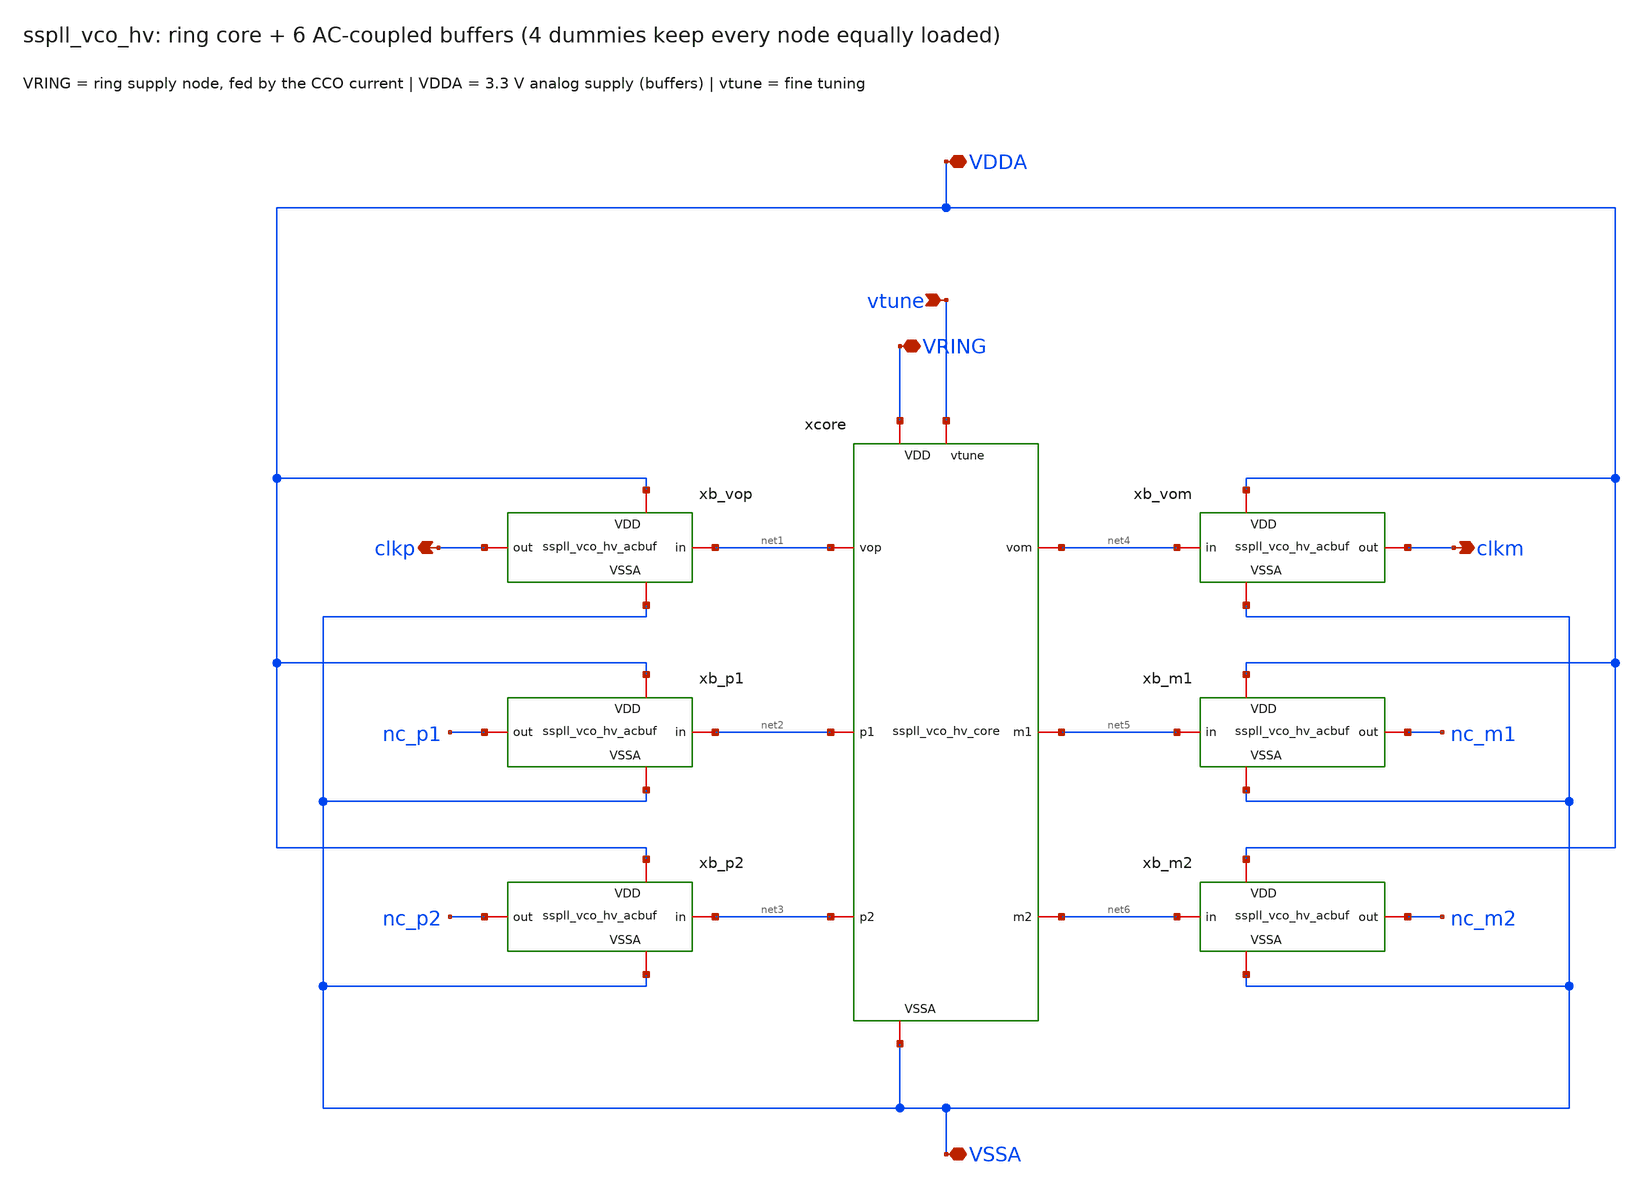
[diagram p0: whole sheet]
** sch_path: xschem/vco_hv/sspll_vco_hv.sch
**.subckt sspll_vco_hv VRING vtune VDDA VSSA clkp clkm
*.iopin VRING
*.ipin vtune
*.iopin VDDA
*.iopin VSSA
*.opin clkp
*.opin clkm
xcore net1 net2 net3 net4 net5 net6 VRING vtune VSSA sspll_vco_hv_core
xb_vop net1 clkp VDDA VSSA sspll_vco_hv_acbuf
xb_p1 net2 nc_p1 VDDA VSSA sspll_vco_hv_acbuf
xb_p2 net3 nc_p2 VDDA VSSA sspll_vco_hv_acbuf
xb_vom net4 clkm VDDA VSSA sspll_vco_hv_acbuf
xb_m1 net5 nc_m1 VDDA VSSA sspll_vco_hv_acbuf
xb_m2 net6 nc_m2 VDDA VSSA sspll_vco_hv_acbuf
**.ends

* expanding   symbol:  sspll_vco_hv_core.sym # of pins=9
** sym_path: xschem/vco_hv/sspll_vco_hv_core.sym
** sch_path: xschem/vco_hv/sspll_vco_hv_core.sch
.subckt sspll_vco_hv_core vop p1 p2 vom m1 m2 VDD vtune VSSA
*.iopin VDD
*.ipin vtune
*.iopin VSSA
*.iopin p1
*.iopin m1
*.iopin p2
*.iopin m2
*.iopin vop
*.iopin vom
x1 vop vom p1 m1 VDD vtune VSSA sspll_vco_hv_dcell
x2 p1 m1 p2 m2 VDD vtune VSSA sspll_vco_hv_dcell
x3 p2 m2 vom vop VDD vtune VSSA sspll_vco_hv_dcell
.ends


* expanding   symbol:  sspll_vco_hv_acbuf.sym # of pins=4
** sym_path: xschem/vco_hv/sspll_vco_hv_acbuf.sym
** sch_path: xschem/vco_hv/sspll_vco_hv_acbuf.sch
.subckt sspll_vco_hv_acbuf in out VDD VSSA
*.iopin VDD
*.iopin VSSA
*.ipin in
*.opin out
XXCC net1 in sky130_fd_pr__cap_mim_m3_1 W=4.2 L=4.2 MF=1 m=1
XXP1 net2 net1 VDD VDD sky130_fd_pr__pfet_g5v0d10v5 L=0.5 W=1.5 nf=1 ad='int((nf+1)/2) * W/nf * 0.29'
+ as='int((nf+2)/2) * W/nf * 0.29' pd='2*int((nf+1)/2) * (W/nf + 0.29)' ps='2*int((nf+2)/2) * (W/nf + 0.29)'
+ nrd='0.29 / W' nrs='0.29 / W' sa=0 sb=0 sd=0 mult=1 m=1
XXN1 net2 net1 VSSA VSSA sky130_fd_pr__nfet_g5v0d10v5 L=0.5 W=0.6 nf=1 ad='int((nf+1)/2) * W/nf * 0.29'
+ as='int((nf+2)/2) * W/nf * 0.29' pd='2*int((nf+1)/2) * (W/nf + 0.29)' ps='2*int((nf+2)/2) * (W/nf + 0.29)'
+ nrd='0.29 / W' nrs='0.29 / W' sa=0 sb=0 sd=0 mult=1 m=1
XXRF net2 net1 VSSA sky130_fd_pr__res_xhigh_po_0p35 L=39.8 mult=1 m=1
XXP2 out net2 VDD VDD sky130_fd_pr__pfet_g5v0d10v5 L=0.5 W=3 nf=1 ad='int((nf+1)/2) * W/nf * 0.29' as='int((nf+2)/2) * W/nf * 0.29'
+ pd='2*int((nf+1)/2) * (W/nf + 0.29)' ps='2*int((nf+2)/2) * (W/nf + 0.29)' nrd='0.29 / W' nrs='0.29 / W'
+ sa=0 sb=0 sd=0 mult=1 m=1
XXN2 out net2 VSSA VSSA sky130_fd_pr__nfet_g5v0d10v5 L=0.5 W=1.2 nf=1 ad='int((nf+1)/2) * W/nf * 0.29'
+ as='int((nf+2)/2) * W/nf * 0.29' pd='2*int((nf+1)/2) * (W/nf + 0.29)' ps='2*int((nf+2)/2) * (W/nf + 0.29)'
+ nrd='0.29 / W' nrs='0.29 / W' sa=0 sb=0 sd=0 mult=1 m=1
.ends


* expanding   symbol:  sspll_vco_hv_dcell.sym # of pins=7
** sym_path: xschem/vco_hv/sspll_vco_hv_dcell.sym
** sch_path: xschem/vco_hv/sspll_vco_hv_dcell.sch
.subckt sspll_vco_hv_dcell inp inm outp outm VDD vtune VSSA
*.iopin VDD
*.iopin VSSA
*.ipin vtune
*.ipin inp
*.ipin inm
*.opin outm
*.opin outp
XXP1 outm inp VDD VDD sky130_fd_pr__pfet_g5v0d10v5 L=0.5 W=25 nf=5 ad='int((nf+1)/2) * W/nf * 0.29' as='int((nf+2)/2) * W/nf * 0.29'
+ pd='2*int((nf+1)/2) * (W/nf + 0.29)' ps='2*int((nf+2)/2) * (W/nf + 0.29)' nrd='0.29 / W' nrs='0.29 / W'
+ sa=0 sb=0 sd=0 mult=1 m=1
XXN1 outm inp VSSA VSSA sky130_fd_pr__nfet_g5v0d10v5 L=0.5 W=7.5 nf=2 ad='int((nf+1)/2) * W/nf * 0.29'
+ as='int((nf+2)/2) * W/nf * 0.29' pd='2*int((nf+1)/2) * (W/nf + 0.29)' ps='2*int((nf+2)/2) * (W/nf + 0.29)'
+ nrd='0.29 / W' nrs='0.29 / W' sa=0 sb=0 sd=0 mult=1 m=1
XXS1 outm vtune net1 VSSA sky130_fd_pr__nfet_g5v0d10v5 L=1.0 W=10 nf=2 ad='int((nf+1)/2) * W/nf * 0.29'
+ as='int((nf+2)/2) * W/nf * 0.29' pd='2*int((nf+1)/2) * (W/nf + 0.29)' ps='2*int((nf+2)/2) * (W/nf + 0.29)'
+ nrd='0.29 / W' nrs='0.29 / W' sa=0 sb=0 sd=0 mult=1 m=1
XXC1 VSSA net1 VSSA VSSA sky130_fd_pr__nfet_g5v0d10v5 L=1.0 W=6.25 nf=1 ad='int((nf+1)/2) * W/nf * 0.29'
+ as='int((nf+2)/2) * W/nf * 0.29' pd='2*int((nf+1)/2) * (W/nf + 0.29)' ps='2*int((nf+2)/2) * (W/nf + 0.29)'
+ nrd='0.29 / W' nrs='0.29 / W' sa=0 sb=0 sd=0 mult=1 m=1
XXP2 outp inm VDD VDD sky130_fd_pr__pfet_g5v0d10v5 L=0.5 W=25 nf=5 ad='int((nf+1)/2) * W/nf * 0.29' as='int((nf+2)/2) * W/nf * 0.29'
+ pd='2*int((nf+1)/2) * (W/nf + 0.29)' ps='2*int((nf+2)/2) * (W/nf + 0.29)' nrd='0.29 / W' nrs='0.29 / W'
+ sa=0 sb=0 sd=0 mult=1 m=1
XXN2 outp inm VSSA VSSA sky130_fd_pr__nfet_g5v0d10v5 L=0.5 W=7.5 nf=2 ad='int((nf+1)/2) * W/nf * 0.29'
+ as='int((nf+2)/2) * W/nf * 0.29' pd='2*int((nf+1)/2) * (W/nf + 0.29)' ps='2*int((nf+2)/2) * (W/nf + 0.29)'
+ nrd='0.29 / W' nrs='0.29 / W' sa=0 sb=0 sd=0 mult=1 m=1
XXS2 outp vtune net2 VSSA sky130_fd_pr__nfet_g5v0d10v5 L=1.0 W=10 nf=2 ad='int((nf+1)/2) * W/nf * 0.29'
+ as='int((nf+2)/2) * W/nf * 0.29' pd='2*int((nf+1)/2) * (W/nf + 0.29)' ps='2*int((nf+2)/2) * (W/nf + 0.29)'
+ nrd='0.29 / W' nrs='0.29 / W' sa=0 sb=0 sd=0 mult=1 m=1
XXC2 VSSA net2 VSSA VSSA sky130_fd_pr__nfet_g5v0d10v5 L=1.0 W=6.25 nf=1 ad='int((nf+1)/2) * W/nf * 0.29'
+ as='int((nf+2)/2) * W/nf * 0.29' pd='2*int((nf+1)/2) * (W/nf + 0.29)' ps='2*int((nf+2)/2) * (W/nf + 0.29)'
+ nrd='0.29 / W' nrs='0.29 / W' sa=0 sb=0 sd=0 mult=1 m=1
XXT1N inp VDD outp VSSA sky130_fd_pr__nfet_g5v0d10v5 L=1.0 W=3.75 nf=2 ad='int((nf+1)/2) * W/nf * 0.29'
+ as='int((nf+2)/2) * W/nf * 0.29' pd='2*int((nf+1)/2) * (W/nf + 0.29)' ps='2*int((nf+2)/2) * (W/nf + 0.29)'
+ nrd='0.29 / W' nrs='0.29 / W' sa=0 sb=0 sd=0 mult=1 m=1
XXT1P outp VSSA inp VDD sky130_fd_pr__pfet_g5v0d10v5 L=0.5 W=7.5 nf=2 ad='int((nf+1)/2) * W/nf * 0.29'
+ as='int((nf+2)/2) * W/nf * 0.29' pd='2*int((nf+1)/2) * (W/nf + 0.29)' ps='2*int((nf+2)/2) * (W/nf + 0.29)'
+ nrd='0.29 / W' nrs='0.29 / W' sa=0 sb=0 sd=0 mult=1 m=1
XXT2N inm VDD outm VSSA sky130_fd_pr__nfet_g5v0d10v5 L=1.0 W=3.75 nf=2 ad='int((nf+1)/2) * W/nf * 0.29'
+ as='int((nf+2)/2) * W/nf * 0.29' pd='2*int((nf+1)/2) * (W/nf + 0.29)' ps='2*int((nf+2)/2) * (W/nf + 0.29)'
+ nrd='0.29 / W' nrs='0.29 / W' sa=0 sb=0 sd=0 mult=1 m=1
XXT2P outm VSSA inm VDD sky130_fd_pr__pfet_g5v0d10v5 L=0.5 W=7.5 nf=2 ad='int((nf+1)/2) * W/nf * 0.29'
+ as='int((nf+2)/2) * W/nf * 0.29' pd='2*int((nf+1)/2) * (W/nf + 0.29)' ps='2*int((nf+2)/2) * (W/nf + 0.29)'
+ nrd='0.29 / W' nrs='0.29 / W' sa=0 sb=0 sd=0 mult=1 m=1
.ends

.end
